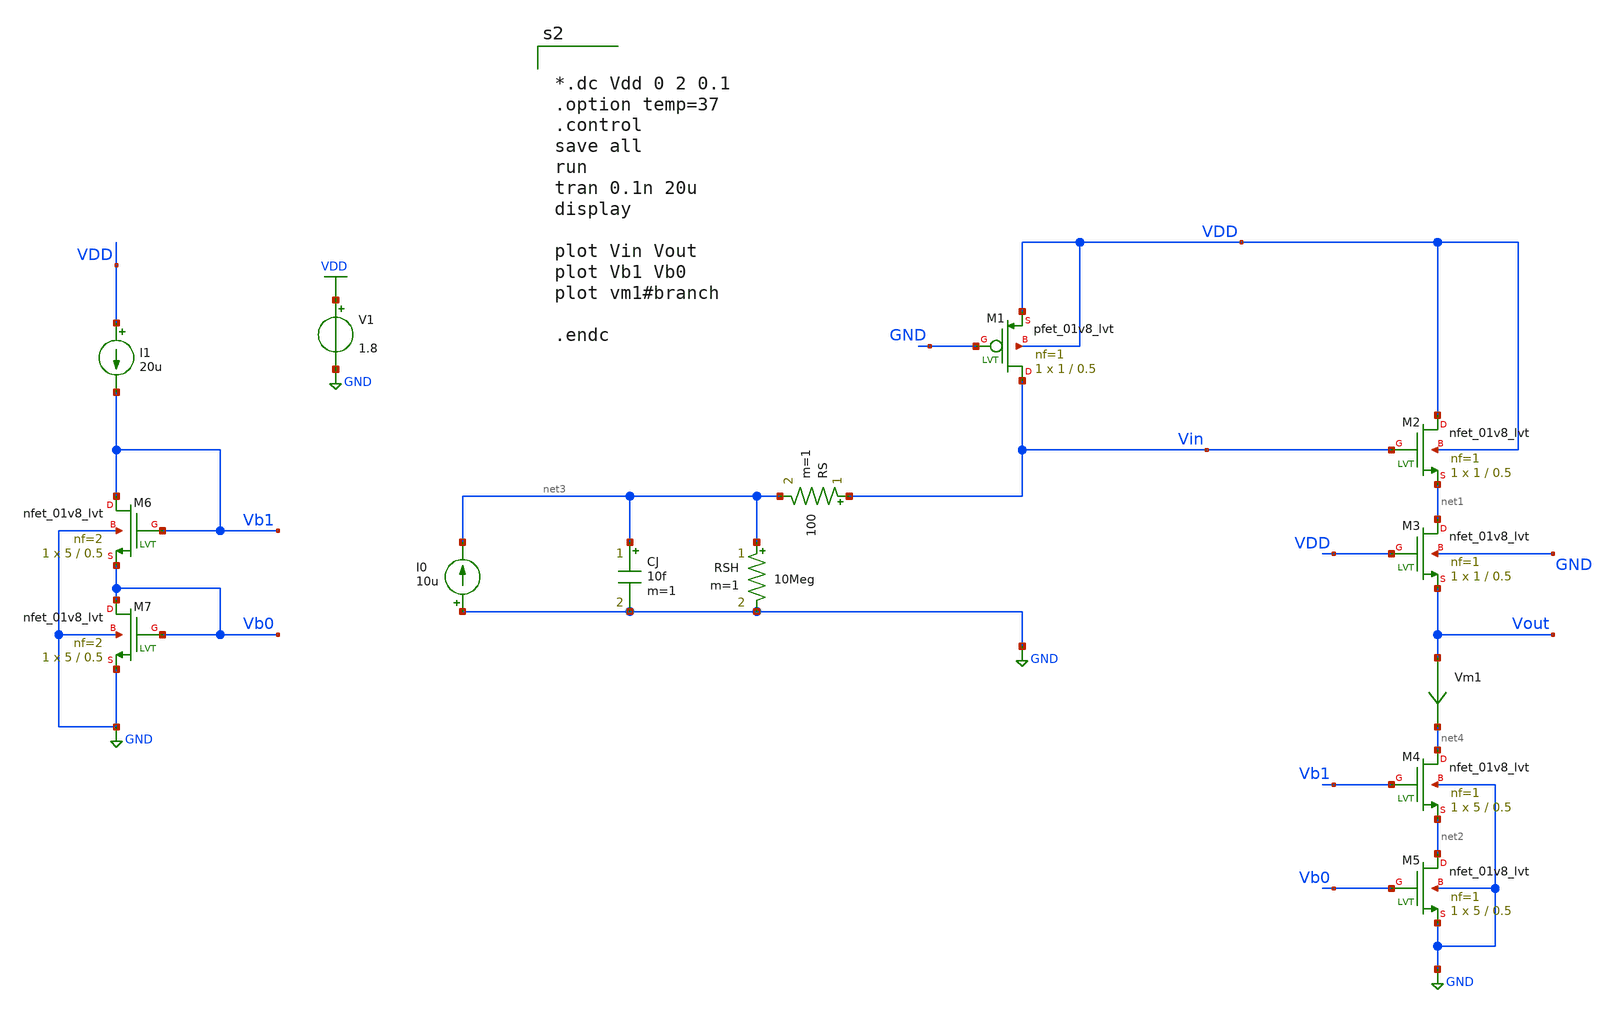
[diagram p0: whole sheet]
** sch_path: xschem/cmos_imager/pixel.sch
**.subckt pixel
XM1 Vin GND VDD VDD sky130_fd_pr__pfet_01v8_lvt L=0.5 W=1 nf=1 ad='int((nf+1)/2) * W/nf * 0.29' as='int((nf+2)/2) * W/nf * 0.29'
+ pd='2*int((nf+1)/2) * (W/nf + 0.29)' ps='2*int((nf+2)/2) * (W/nf + 0.29)' nrd='0.29 / W' nrs='0.29 / W'
+ sa=0 sb=0 sd=0 mult=1 m=1
XM2 VDD Vin net1 VDD sky130_fd_pr__nfet_01v8_lvt L=0.5 W=1 nf=1 ad='int((nf+1)/2) * W/nf * 0.29' as='int((nf+2)/2) * W/nf * 0.29'
+ pd='2*int((nf+1)/2) * (W/nf + 0.29)' ps='2*int((nf+2)/2) * (W/nf + 0.29)' nrd='0.29 / W' nrs='0.29 / W'
+ sa=0 sb=0 sd=0 mult=1 m=1
XM3 net1 VDD Vout GND sky130_fd_pr__nfet_01v8_lvt L=0.5 W=1 nf=1 ad='int((nf+1)/2) * W/nf * 0.29' as='int((nf+2)/2) * W/nf * 0.29'
+ pd='2*int((nf+1)/2) * (W/nf + 0.29)' ps='2*int((nf+2)/2) * (W/nf + 0.29)' nrd='0.29 / W' nrs='0.29 / W'
+ sa=0 sb=0 sd=0 mult=1 m=1
XM4 net4 Vb1 net2 GND sky130_fd_pr__nfet_01v8_lvt L=0.5 W=5 nf=1 ad='int((nf+1)/2) * W/nf * 0.29' as='int((nf+2)/2) * W/nf * 0.29'
+ pd='2*int((nf+1)/2) * (W/nf + 0.29)' ps='2*int((nf+2)/2) * (W/nf + 0.29)' nrd='0.29 / W' nrs='0.29 / W'
+ sa=0 sb=0 sd=0 mult=1 m=1
XM5 net2 Vb0 GND GND sky130_fd_pr__nfet_01v8_lvt L=0.5 W=5 nf=1 ad='int((nf+1)/2) * W/nf * 0.29' as='int((nf+2)/2) * W/nf * 0.29'
+ pd='2*int((nf+1)/2) * (W/nf + 0.29)' ps='2*int((nf+2)/2) * (W/nf + 0.29)' nrd='0.29 / W' nrs='0.29 / W'
+ sa=0 sb=0 sd=0 mult=1 m=1
I0 GND net3 10u
CJ net3 GND 10f m=1
RSH net3 GND 10Meg m=1
RS Vin net3 100 m=1
XM6 Vb1 Vb1 Vb0 GND sky130_fd_pr__nfet_01v8_lvt L=0.5 W=5 nf=2 ad='int((nf+1)/2) * W/nf * 0.29' as='int((nf+2)/2) * W/nf * 0.29'
+ pd='2*int((nf+1)/2) * (W/nf + 0.29)' ps='2*int((nf+2)/2) * (W/nf + 0.29)' nrd='0.29 / W' nrs='0.29 / W'
+ sa=0 sb=0 sd=0 mult=1 m=1
XM7 Vb0 Vb0 GND GND sky130_fd_pr__nfet_01v8_lvt L=0.5 W=5 nf=2 ad='int((nf+1)/2) * W/nf * 0.29' as='int((nf+2)/2) * W/nf * 0.29'
+ pd='2*int((nf+1)/2) * (W/nf + 0.29)' ps='2*int((nf+2)/2) * (W/nf + 0.29)' nrd='0.29 / W' nrs='0.29 / W'
+ sa=0 sb=0 sd=0 mult=1 m=1
I1 VDD Vb1 20u
V1 VDD GND 1.8
Vm1 Vout net4 0
.save i(vm1)
**** begin user architecture code

** opencircuitdesign pdks install
.lib $::SKYWATER_MODELS/sky130.lib.spice tt




*.dc Vdd 0 2 0.1
.option temp=37
.control
save all
run
tran 0.1n 20u
display

plot Vin Vout
plot Vb1 Vb0
plot vm1#branch

.endc


**** end user architecture code
**.ends
.GLOBAL GND
.GLOBAL VDD
.end
